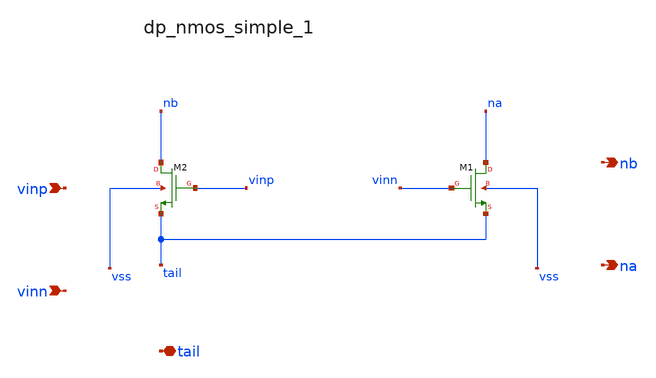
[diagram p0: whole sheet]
** sch_path: analog-db/raw/amp_019_ti_ldo_error/hier/blocks/dp_nmos_simple_1.sch
**.subckt dp_nmos_simple_1 vinp vinn tail nb na
*.ipin vinp
*.ipin vinn
*.iopin tail
*.opin nb
*.opin na
XM1 na vinn tail vss sg13_hv_nmos w=x_dut_xm1_w l=x_dut_xm1_l ng=1 m=1
XM2 nb vinp tail vss sg13_hv_nmos w=x_dut_xm2_w l=x_dut_xm2_l ng=1 m=1
**.ends
.end
